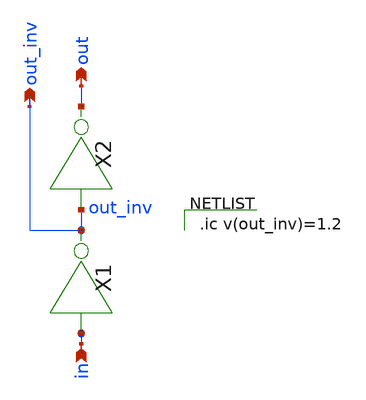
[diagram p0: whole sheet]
** sch_path: xschem/decoder/bottom_peripheral_cell.sch
**.subckt bottom_peripheral_cell in out out_inv in
*.ipin in
*.opin out
*.opin out_inv
*.ipin in
X2 out_inv out inv
X1 in out_inv inv
**** begin user architecture code

.ic v(out_inv)=1.2

**** end user architecture code
**.ends

* expanding   symbol:  inv/inv.sym # of pins=2
** sym_path: xschem/inv/inv.sym
** sch_path: xschem/inv/inv.sch
.subckt inv in out
*.ipin in
*.iopin out
XM1 out in GND GND sky130_fd_pr__nfet_01v8 L=0.18 W=0.5 nf=1 ad='int((nf+1)/2) * W/nf * 0.29' as='int((nf+2)/2) * W/nf * 0.29'
+ pd='2*int((nf+1)/2) * (W/nf + 0.29)' ps='2*int((nf+2)/2) * (W/nf + 0.29)' nrd='0.29 / W' nrs='0.29 / W'
+ sa=0 sb=0 sd=0 mult=1 m=1
XM2 out in VDD VDD sky130_fd_pr__pfet_01v8 L=0.18 W=1 nf=1 ad='int((nf+1)/2) * W/nf * 0.29' as='int((nf+2)/2) * W/nf * 0.29'
+ pd='2*int((nf+1)/2) * (W/nf + 0.29)' ps='2*int((nf+2)/2) * (W/nf + 0.29)' nrd='0.29 / W' nrs='0.29 / W'
+ sa=0 sb=0 sd=0 mult=1 m=1
.ends

.GLOBAL VDD
.GLOBAL GND
.end
